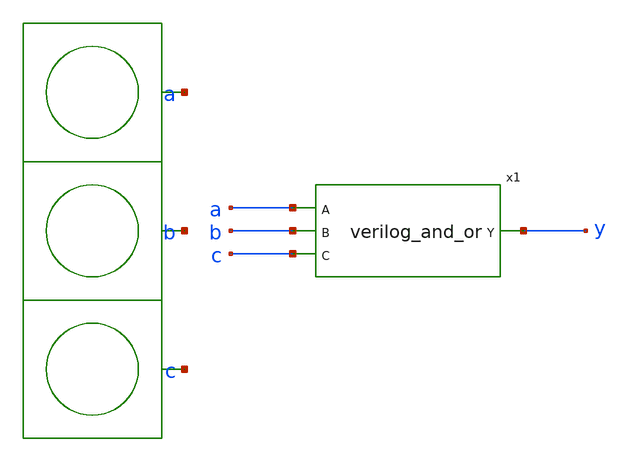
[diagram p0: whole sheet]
** sch_path: project/examples/verilog_and_or/verilog_and_or_testbench.sch
**.subckt verilog_and_or_testbench
x1 a b c y VGND VNB VPB VPWR verilog_and_or
VBUTTON_A a VGND external
VBUTTON_B b VGND external
VBUTTON_C c VGND external
**.ends
.end
